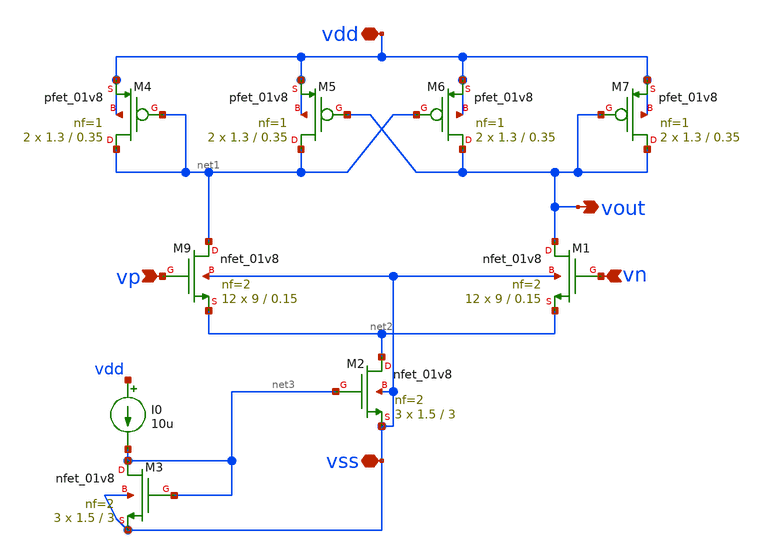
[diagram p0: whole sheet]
** sch_path: designs/subcells/core_opampr/opamp_r.sch
**.subckt opamp_r vdd vout vp vss vn
*.iopin vdd
*.opin vout
*.ipin vp
*.iopin vss
*.ipin vn
I0 vdd net3 10u
XM9 net1 vp net2 vss sky130_fd_pr__nfet_01v8 L=0.15 W=9 nf=2 ad='int((2 + 1)/2) * 9 / 2 * 0.29' as='int((2 + 2)/2) * 9 / 2 * 0.29'
+ pd='2*int((2 + 1)/2) * (9 / 2 + 0.29)' ps='2*int((2 + 2)/2) * (9 / 2 + 0.29)' nrd='0.29 / 9 ' nrs='0.29 / 9 '
+ sa=0 sb=0 sd=0 mult=12 m=12
XM4 net1 net1 vdd vdd sky130_fd_pr__pfet_01v8 L=0.35 W=1.3 nf=1 ad='int((nf+1)/2) * W/nf * 0.29' as='int((nf+2)/2) * W/nf * 0.29'
+ pd='2*int((nf+1)/2) * (W/nf + 0.29)' ps='2*int((nf+2)/2) * (W/nf + 0.29)' nrd='0.29 / W' nrs='0.29 / W'
+ sa=0 sb=0 sd=0 mult=2 m=2
XM5 net1 vout vdd vdd sky130_fd_pr__pfet_01v8 L=0.35 W=1.3 nf=1 ad='int((nf+1)/2) * W/nf * 0.29' as='int((nf+2)/2) * W/nf * 0.29'
+ pd='2*int((nf+1)/2) * (W/nf + 0.29)' ps='2*int((nf+2)/2) * (W/nf + 0.29)' nrd='0.29 / W' nrs='0.29 / W'
+ sa=0 sb=0 sd=0 mult=2 m=2
XM6 vout net1 vdd vdd sky130_fd_pr__pfet_01v8 L=0.35 W=1.3 nf=1 ad='int((nf+1)/2) * W/nf * 0.29' as='int((nf+2)/2) * W/nf * 0.29'
+ pd='2*int((nf+1)/2) * (W/nf + 0.29)' ps='2*int((nf+2)/2) * (W/nf + 0.29)' nrd='0.29 / W' nrs='0.29 / W'
+ sa=0 sb=0 sd=0 mult=2 m=2
XM7 vout vout vdd vdd sky130_fd_pr__pfet_01v8 L=0.35 W=1.3 nf=1 ad='int((nf+1)/2) * W/nf * 0.29' as='int((nf+2)/2) * W/nf * 0.29'
+ pd='2*int((nf+1)/2) * (W/nf + 0.29)' ps='2*int((nf+2)/2) * (W/nf + 0.29)' nrd='0.29 / W' nrs='0.29 / W'
+ sa=0 sb=0 sd=0 mult=2 m=2
XM1 vout vn net2 vss sky130_fd_pr__nfet_01v8 L=0.15 W=9 nf=2 ad='int((2 + 1)/2) * 9 / 2 * 0.29' as='int((2 + 2)/2) * 9 / 2 * 0.29'
+ pd='2*int((2 + 1)/2) * (9 / 2 + 0.29)' ps='2*int((2 + 2)/2) * (9 / 2 + 0.29)' nrd='0.29 / 9 ' nrs='0.29 / 9 '
+ sa=0 sb=0 sd=0 mult=12 m=12
XM2 net2 net3 vss vss sky130_fd_pr__nfet_01v8 L=3 W=1.5 nf=2 ad='int((2 + 1)/2) * 1.5 / 2 * 0.29' as='int((2 + 2)/2) * 1.5 / 2 * 0.29'
+ pd='2*int((2 + 1)/2) * (1.5 / 2 + 0.29)' ps='2*int((2 + 2)/2) * (1.5 / 2 + 0.29)' nrd='0.29 / 1.5 ' nrs='0.29 / 1.5 '
+ sa=0 sb=0 sd=0 mult=3 m=3
XM3 net3 net3 vss vss sky130_fd_pr__nfet_01v8 L=3 W=1.5 nf=2 ad='int((2 + 1)/2) * 1.5 / 2 * 0.29' as='int((2 + 2)/2) * 1.5 / 2 * 0.29'
+ pd='2*int((2 + 1)/2) * (1.5 / 2 + 0.29)' ps='2*int((2 + 2)/2) * (1.5 / 2 + 0.29)' nrd='0.29 / 1.5 ' nrs='0.29 / 1.5 '
+ sa=0 sb=0 sd=0 mult=3 m=3
**.ends
.end
